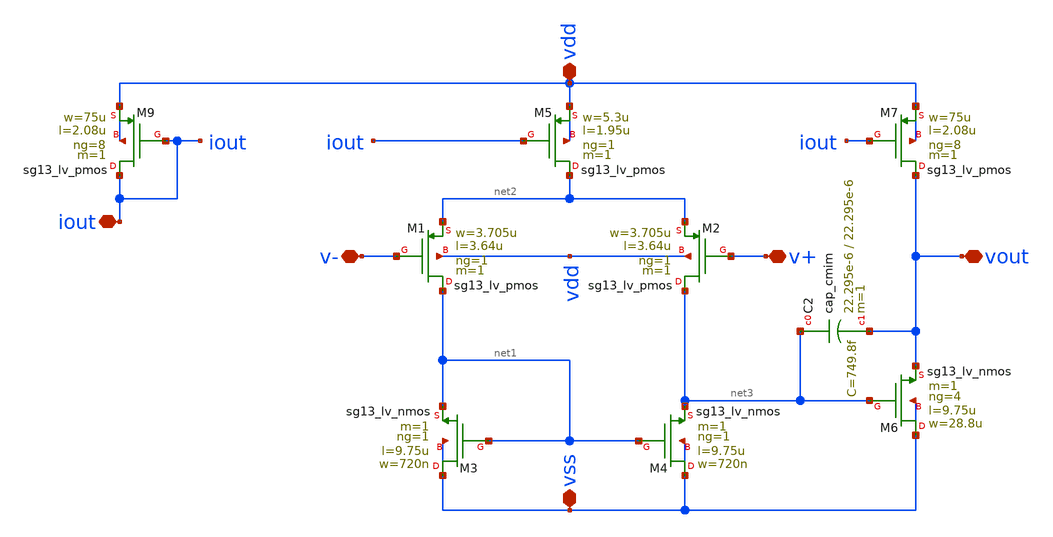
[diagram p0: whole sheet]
** sch_path: modules/module_1_bandgap_reference/part_1_OTA/schematic/two_stage_OTA.sch
**.subckt two_stage_OTA v- v+ vss vdd iout vout
*.iopin v-
*.iopin v+
*.iopin vss
*.iopin vdd
*.iopin iout
*.iopin vout
XM4 vss net1 net3 vss sg13_lv_nmos w=720n l=9.75u ng=1 m=1 mm_ok=1
XM3 vss net1 net1 vss sg13_lv_nmos w=720n l=9.75u ng=1 m=1 mm_ok=1
XM1 net1 v- net2 vdd sg13_lv_pmos w=3.705u l=3.64u ng=1 m=1 mm_ok=1
XM2 net3 v+ net2 vdd sg13_lv_pmos w=3.705u l=3.64u ng=1 m=1 mm_ok=1
XM5 net2 iout vdd vdd sg13_lv_pmos w=5.3u l=1.95u ng=1 m=1 mm_ok=1
XM7 vout iout vdd vdd sg13_lv_pmos w=75u l=2.08u ng=8 m=1 mm_ok=1
XM6 vss net3 vout vss sg13_lv_nmos w=28.8u l=9.75u ng=4 m=1 mm_ok=1
XM9 iout iout vdd vdd sg13_lv_pmos w=75u l=2.08u ng=8 m=1 mm_ok=1
XC2 net3 vout cap_cmim w=22.295e-6 l=22.295e-6 m=1 mm_ok=1
**.ends
.end
